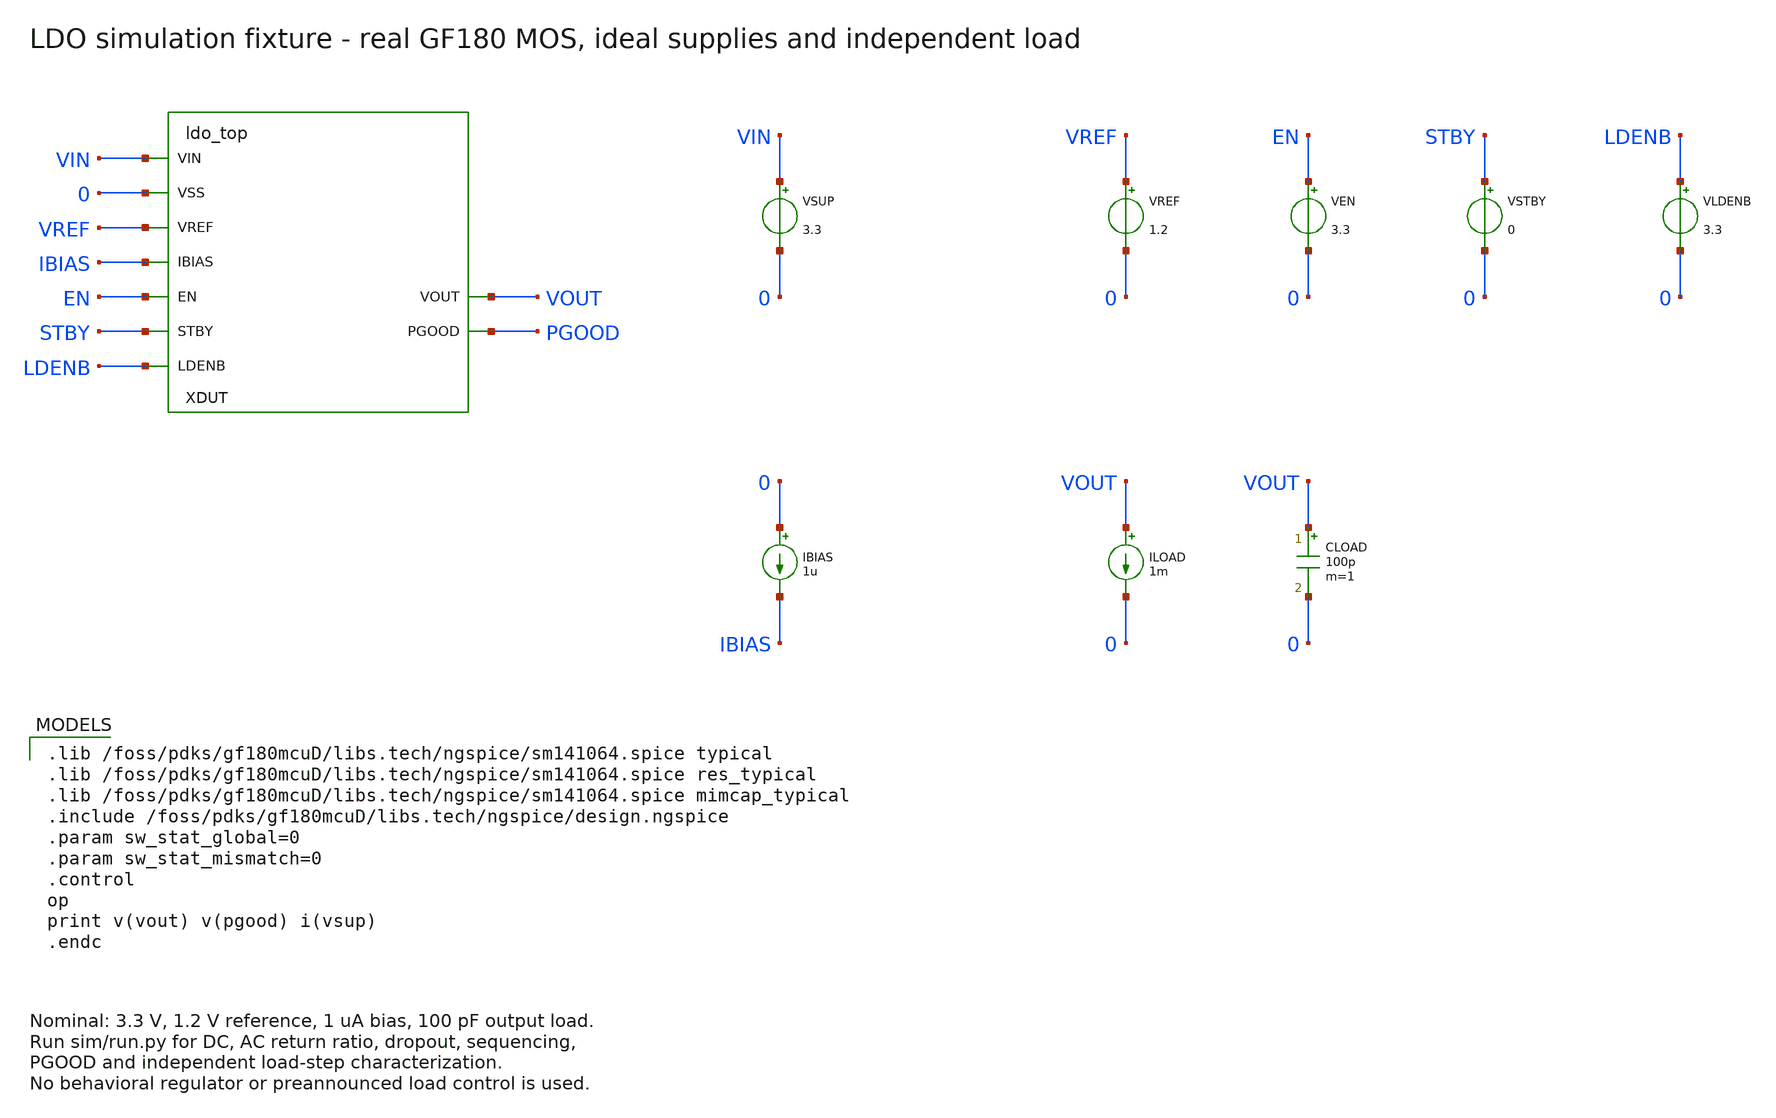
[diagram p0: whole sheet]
** sch_path: schematics/ldo_tb.sch
**.subckt ldo_tb
XDUT VIN 0 VREF IBIAS EN STBY LDENB VOUT PGOOD ldo_top
VLDENB LDENB 0 3.3
VSUP VIN 0 3.3
VREF VREF 0 1.2
VEN EN 0 3.3
VSTBY STBY 0 0
IBIAS 0 IBIAS 1u
ILOAD VOUT 0 1m
CLOAD VOUT 0 100p m=1
**** begin user architecture code

.lib /foss/pdks/gf180mcuD/libs.tech/ngspice/sm141064.spice typical
.lib /foss/pdks/gf180mcuD/libs.tech/ngspice/sm141064.spice res_typical
.lib /foss/pdks/gf180mcuD/libs.tech/ngspice/sm141064.spice mimcap_typical
.include /foss/pdks/gf180mcuD/libs.tech/ngspice/design.ngspice
.param sw_stat_global=0
.param sw_stat_mismatch=0
.control
op
print v(vout) v(pgood) i(vsup)
.endc

**** end user architecture code
**.ends
.end
